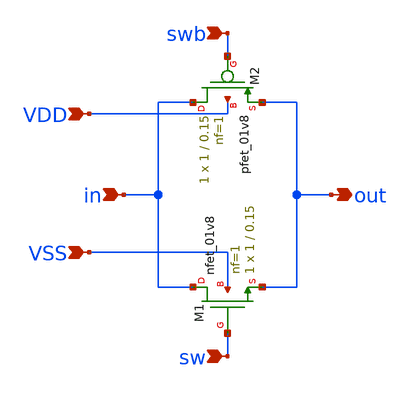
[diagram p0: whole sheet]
** sch_path: hgu/xschem/hgu_sw_vref_gen.sch
**.subckt hgu_sw_vref_gen in out sw swb VDD VSS
*.ipin in
*.opin out
*.ipin sw
*.ipin swb
*.ipin VDD
*.ipin VSS
XM1 in sw out VSS sky130_fd_pr__nfet_01v8 L=0.15 W=1 nf=1 ad='int((nf+1)/2) * W/nf * 0.29' as='int((nf+2)/2) * W/nf * 0.29'
+ pd='2*int((nf+1)/2) * (W/nf + 0.29)' ps='2*int((nf+2)/2) * (W/nf + 0.29)' nrd='0.29 / W' nrs='0.29 / W'
+ sa=0 sb=0 sd=0 mult=1 m=1
XM2 in swb out VDD sky130_fd_pr__pfet_01v8 L=0.15 W=1 nf=1 ad='int((nf+1)/2) * W/nf * 0.29' as='int((nf+2)/2) * W/nf * 0.29'
+ pd='2*int((nf+1)/2) * (W/nf + 0.29)' ps='2*int((nf+2)/2) * (W/nf + 0.29)' nrd='0.29 / W' nrs='0.29 / W'
+ sa=0 sb=0 sd=0 mult=1 m=1
**.ends
.end
